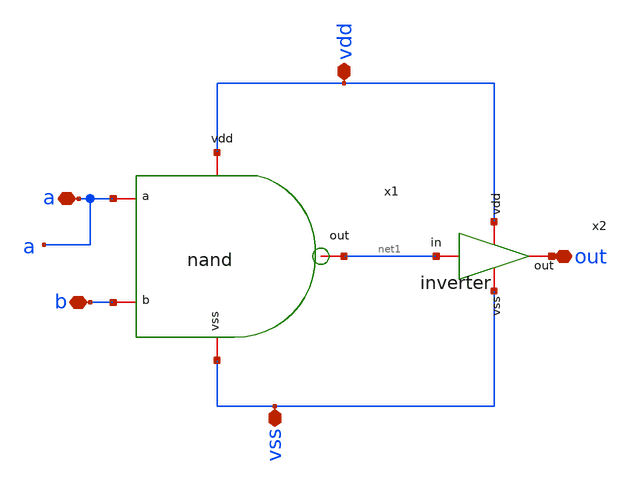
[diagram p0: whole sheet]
** sch_path: design/blocks/andgate/schematic/andgate.sch
**.subckt andgate a b vss vdd out
*.iopin a
*.iopin b
*.iopin vss
*.iopin vdd
*.iopin out
x1 a b net1 vss vdd nand
x2 vdd out net1 vss inverter
**.ends

* expanding   symbol:  blocks/nandgate/schematic/nand.sym # of pins=5
** sym_path: design/blocks/nandgate/schematic/nand.sym
** sch_path: design/blocks/nandgate/schematic/nand.sch
.subckt nand a b out vss vdd
*.iopin vdd
*.iopin a
*.iopin vss
*.iopin out
*.iopin b
XM1 out a vdd net2 sg13_lv_pmos w=0.15u l=0.13u ng=1 m=1 mm_ok=1
XM2 out a net1 net3 sg13_lv_nmos w=0.15u l=0.13u ng=1 m=1 mm_ok=1
XM3 net1 b net4 net5 sg13_lv_nmos w=0.15u l=0.13u ng=1 m=1 mm_ok=1
XM4 out b vdd net6 sg13_lv_pmos w=0.15u l=0.13u ng=1 m=1 mm_ok=1
.ends


* expanding   symbol:  blocks/inverter/schematic/inverter.sym # of pins=4
** sym_path: design/blocks/inverter/schematic/inverter.sym
** sch_path: design/blocks/inverter/schematic/inverter.sch
.subckt inverter vdd out in vss
*.iopin vdd
*.iopin out
*.iopin vss
*.iopin in
XM1 out in vss vss sg13_lv_nmos w=0.75u l=0.15u ng=1 m=1 mm_ok=1
XM2 out in vdd vdd sg13_lv_pmos w=1.5u l=0.15u ng=1 m=1 mm_ok=1
.ends

.end
